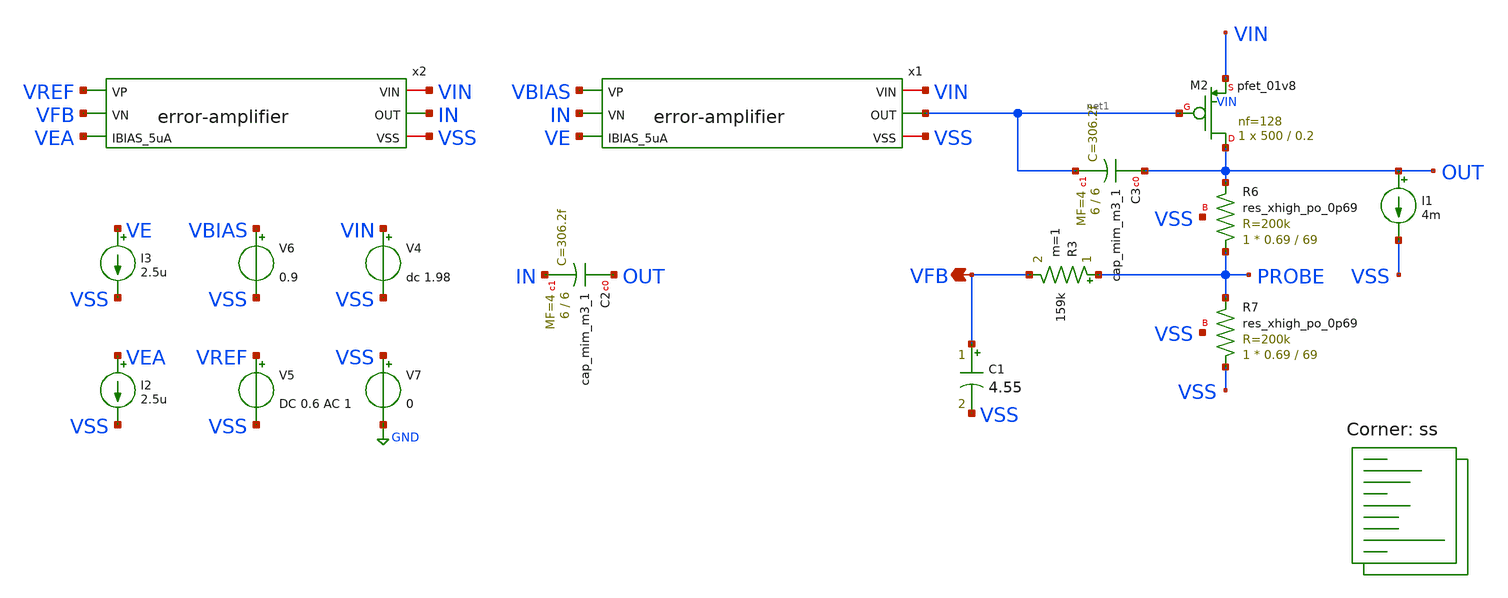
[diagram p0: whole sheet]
** sch_path: xschem/ldo_andriansyah/testbench/loop-gain.sch
**.subckt loop-gain VFB
*.opin VFB
R3 PROBE VFB 159k m=1
C1 VFB VSS 4.55 m=1
XC2 OUT IN sky130_fd_pr__cap_mim_m3_1 W=6 L=6 MF=4 m=4
XC3 OUT net1 sky130_fd_pr__cap_mim_m3_1 W=6 L=6 MF=4 m=4
x2 VIN VREF VFB VEA IN VSS error-amplifier
XR6 PROBE OUT VSS sky130_fd_pr__res_xhigh_po_0p69 L=69 mult=1 m=1
XR7 VSS PROBE VSS sky130_fd_pr__res_xhigh_po_0p69 L=69 mult=1 m=1
XM2 OUT net1 VIN VIN sky130_fd_pr__pfet_01v8 L=0.2 W=500 nf=128 ad='int((nf+1)/2) * W/nf * 0.29' as='int((nf+2)/2) * W/nf * 0.29'
+ pd='2*int((nf+1)/2) * (W/nf + 0.29)' ps='2*int((nf+2)/2) * (W/nf + 0.29)' nrd='0.29 / W' nrs='0.29 / W'
+ sa=0 sb=0 sd=0 mult=1 m=1
I1 OUT VSS 4m
x1 VIN VBIAS IN VE net1 VSS error-amplifier
V7 VSS GND 0
V4 VIN VSS dc 1.98
V5 VREF VSS DC 0.6 AC 1
I2 VEA VSS 2.5u
V6 VBIAS VSS 0.9
I3 VE VSS 2.5u
**** begin user architecture code
.lib $::SKYWATER_MODELS/sky130.lib.spice ss



.temp 125
.control
ac dec 20 1 100meg

let gain_db = db(v(PROBE))
let phase_deg = ph(v(PROBE)) * 180/PI

meas ac ugf when gain_db=0 fall=1
meas ac phase_at_ugf find phase_deg at=ugf

* Wrap phase into (-360, 0] so PM math is consistent regardless of branch
let phase_wrapped = phase_at_ugf
if phase_wrapped > 180
  let phase_wrapped = phase_wrapped - 360
end
if phase_wrapped < -180
  let phase_wrapped = phase_wrapped + 360
end

let pm_actual = 180 + phase_wrapped

echo Unity Gain Frequency: $&ugf Hz
echo Raw phase at UGF:     $&phase_at_ugf Degrees
echo Unwrapped phase:      $&phase_wrapped Degrees
echo Calculated Phase Margin: $&pm_actual Degrees

plot gain_db phase_deg

.endc




**** end user architecture code
**.ends

* expanding   symbol:
*+  /foss/designs/2026/tt_sky26b_ldo_andriansyah/xschem/error-amplifier/error-amplifier.sym # of pins=6
** sym_path: xschem/error-amplifier/error-amplifier.sym
** sch_path: xschem/error-amplifier/error-amplifier.sch
.subckt error-amplifier VIN VP VN IBIAS_5uA OUT VSS
*.ipin IBIAS_5uA
*.ipin VN
*.ipin VP
*.iopin VIN
*.iopin VSS
*.opin OUT
XM1 net2 net2 VSS VSS sky130_fd_pr__nfet_01v8 L=0.6 W=4.2 nf=4 ad='int((nf+1)/2) * W/nf * 0.29' as='int((nf+2)/2) * W/nf * 0.29'
+ pd='2*int((nf+1)/2) * (W/nf + 0.29)' ps='2*int((nf+2)/2) * (W/nf + 0.29)' nrd='0.29 / W' nrs='0.29 / W'
+ sa=0 sb=0 sd=0 mult=1 m=1
XM2 OUT net2 VSS VSS sky130_fd_pr__nfet_01v8 L=0.6 W=4.2 nf=4 ad='int((nf+1)/2) * W/nf * 0.29' as='int((nf+2)/2) * W/nf * 0.29'
+ pd='2*int((nf+1)/2) * (W/nf + 0.29)' ps='2*int((nf+2)/2) * (W/nf + 0.29)' nrd='0.29 / W' nrs='0.29 / W'
+ sa=0 sb=0 sd=0 mult=1 m=1
XM3 net2 VN net1 VDD sky130_fd_pr__pfet_01v8 L=0.6 W=28 nf=4 ad='int((nf+1)/2) * W/nf * 0.29' as='int((nf+2)/2) * W/nf * 0.29'
+ pd='2*int((nf+1)/2) * (W/nf + 0.29)' ps='2*int((nf+2)/2) * (W/nf + 0.29)' nrd='0.29 / W' nrs='0.29 / W'
+ sa=0 sb=0 sd=0 mult=1 m=1
XM4 OUT VP net1 VDD sky130_fd_pr__pfet_01v8 L=0.6 W=28 nf=4 ad='int((nf+1)/2) * W/nf * 0.29' as='int((nf+2)/2) * W/nf * 0.29'
+ pd='2*int((nf+1)/2) * (W/nf + 0.29)' ps='2*int((nf+2)/2) * (W/nf + 0.29)' nrd='0.29 / W' nrs='0.29 / W'
+ sa=0 sb=0 sd=0 mult=1 m=1
XM5 net1 IBIAS_5uA VIN VIN sky130_fd_pr__pfet_01v8 L=0.6 W=6.6 nf=4 ad='int((nf+1)/2) * W/nf * 0.29'
+ as='int((nf+2)/2) * W/nf * 0.29' pd='2*int((nf+1)/2) * (W/nf + 0.29)' ps='2*int((nf+2)/2) * (W/nf + 0.29)'
+ nrd='0.29 / W' nrs='0.29 / W' sa=0 sb=0 sd=0 mult=1 m=1
XM6 IBIAS_5uA IBIAS_5uA VIN VIN sky130_fd_pr__pfet_01v8 L=0.6 W=6.6 nf=4 ad='int((nf+1)/2) * W/nf * 0.29'
+ as='int((nf+2)/2) * W/nf * 0.29' pd='2*int((nf+1)/2) * (W/nf + 0.29)' ps='2*int((nf+2)/2) * (W/nf + 0.29)'
+ nrd='0.29 / W' nrs='0.29 / W' sa=0 sb=0 sd=0 mult=1 m=1
XM7 VDD VDD VDD VDD sky130_fd_pr__pfet_01v8 L=0.6 W=7 nf=1 ad='int((nf+1)/2) * W/nf * 0.29' as='int((nf+2)/2) * W/nf * 0.29'
+ pd='2*int((nf+1)/2) * (W/nf + 0.29)' ps='2*int((nf+2)/2) * (W/nf + 0.29)' nrd='0.29 / W' nrs='0.29 / W'
+ sa=0 sb=0 sd=0 mult=1 m=1
XM8 VSS VSS VSS VSS sky130_fd_pr__nfet_01v8 L=0.6 W=1.05 nf=1 ad='int((nf+1)/2) * W/nf * 0.29' as='int((nf+2)/2) * W/nf * 0.29'
+ pd='2*int((nf+1)/2) * (W/nf + 0.29)' ps='2*int((nf+2)/2) * (W/nf + 0.29)' nrd='0.29 / W' nrs='0.29 / W'
+ sa=0 sb=0 sd=0 mult=1 m=1
XM9 VDD VDD VDD VDD sky130_fd_pr__pfet_01v8 L=0.6 W=1.65 nf=1 ad='int((nf+1)/2) * W/nf * 0.29' as='int((nf+2)/2) * W/nf * 0.29'
+ pd='2*int((nf+1)/2) * (W/nf + 0.29)' ps='2*int((nf+2)/2) * (W/nf + 0.29)' nrd='0.29 / W' nrs='0.29 / W'
+ sa=0 sb=0 sd=0 mult=1 m=1
XM10 VSS VSS VSS VSS sky130_fd_pr__nfet_01v8 L=0.6 W=1.05 nf=1 ad='int((nf+1)/2) * W/nf * 0.29' as='int((nf+2)/2) * W/nf * 0.29'
+ pd='2*int((nf+1)/2) * (W/nf + 0.29)' ps='2*int((nf+2)/2) * (W/nf + 0.29)' nrd='0.29 / W' nrs='0.29 / W'
+ sa=0 sb=0 sd=0 mult=1 m=1
XM11 VDD VDD VDD VDD sky130_fd_pr__pfet_01v8 L=0.6 W=7 nf=1 ad='int((nf+1)/2) * W/nf * 0.29' as='int((nf+2)/2) * W/nf * 0.29'
+ pd='2*int((nf+1)/2) * (W/nf + 0.29)' ps='2*int((nf+2)/2) * (W/nf + 0.29)' nrd='0.29 / W' nrs='0.29 / W'
+ sa=0 sb=0 sd=0 mult=1 m=1
XM12 VDD VDD VDD VDD sky130_fd_pr__pfet_01v8 L=0.6 W=1.65 nf=1 ad='int((nf+1)/2) * W/nf * 0.29' as='int((nf+2)/2) * W/nf * 0.29'
+ pd='2*int((nf+1)/2) * (W/nf + 0.29)' ps='2*int((nf+2)/2) * (W/nf + 0.29)' nrd='0.29 / W' nrs='0.29 / W'
+ sa=0 sb=0 sd=0 mult=1 m=1
.ends

.GLOBAL GND
.end
